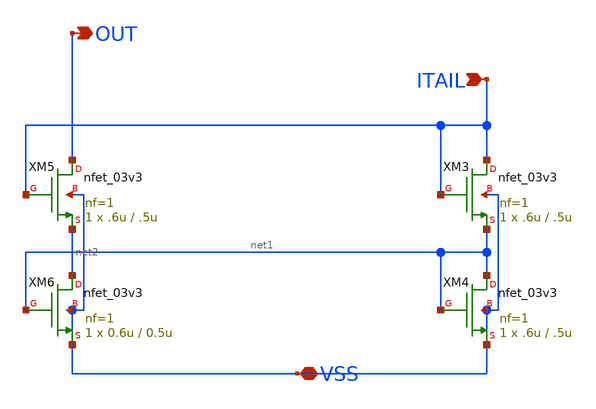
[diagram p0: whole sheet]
** sch_path: DAC_PAKISTAN_01/Pakistan1_Xschem/untitled-13.sch
**.subckt untitled-13 OUT ITAIL VSS
*.opin OUT
*.ipin ITAIL
*.iopin VSS
XM3 ITAIL ITAIL net1 VSS nfet_03v3 L=.5u W=.6u nf=1 ad='int((nf+1)/2) * W/nf * 0.18u' as='int((nf+2)/2) * W/nf * 0.18u'
+ pd='2*int((nf+1)/2) * (W/nf + 0.18u)' ps='2*int((nf+2)/2) * (W/nf + 0.18u)' nrd='0.18u / W' nrs='0.18u / W'
+ sa=0 sb=0 sd=0 m=1
XM4 net1 net1 VSS VSS nfet_03v3 L=.5u W=.6u nf=1 ad='int((nf+1)/2) * W/nf * 0.18u' as='int((nf+2)/2) * W/nf * 0.18u'
+ pd='2*int((nf+1)/2) * (W/nf + 0.18u)' ps='2*int((nf+2)/2) * (W/nf + 0.18u)' nrd='0.18u / W' nrs='0.18u / W'
+ sa=0 sb=0 sd=0 m=1
XM5 OUT ITAIL net2 VSS nfet_03v3 L=.5u W=.6u nf=1 ad='int((nf+1)/2) * W/nf * 0.18u' as='int((nf+2)/2) * W/nf * 0.18u'
+ pd='2*int((nf+1)/2) * (W/nf + 0.18u)' ps='2*int((nf+2)/2) * (W/nf + 0.18u)' nrd='0.18u / W' nrs='0.18u / W'
+ sa=0 sb=0 sd=0 m=1
XM6 net2 net1 VSS VSS nfet_03v3 L=0.5u W=0.6u nf=1 ad='int((nf+1)/2) * W/nf * 0.18u' as='int((nf+2)/2) * W/nf * 0.18u'
+ pd='2*int((nf+1)/2) * (W/nf + 0.18u)' ps='2*int((nf+2)/2) * (W/nf + 0.18u)' nrd='0.18u / W' nrs='0.18u / W'
+ sa=0 sb=0 sd=0 m=1
**.ends
.end
